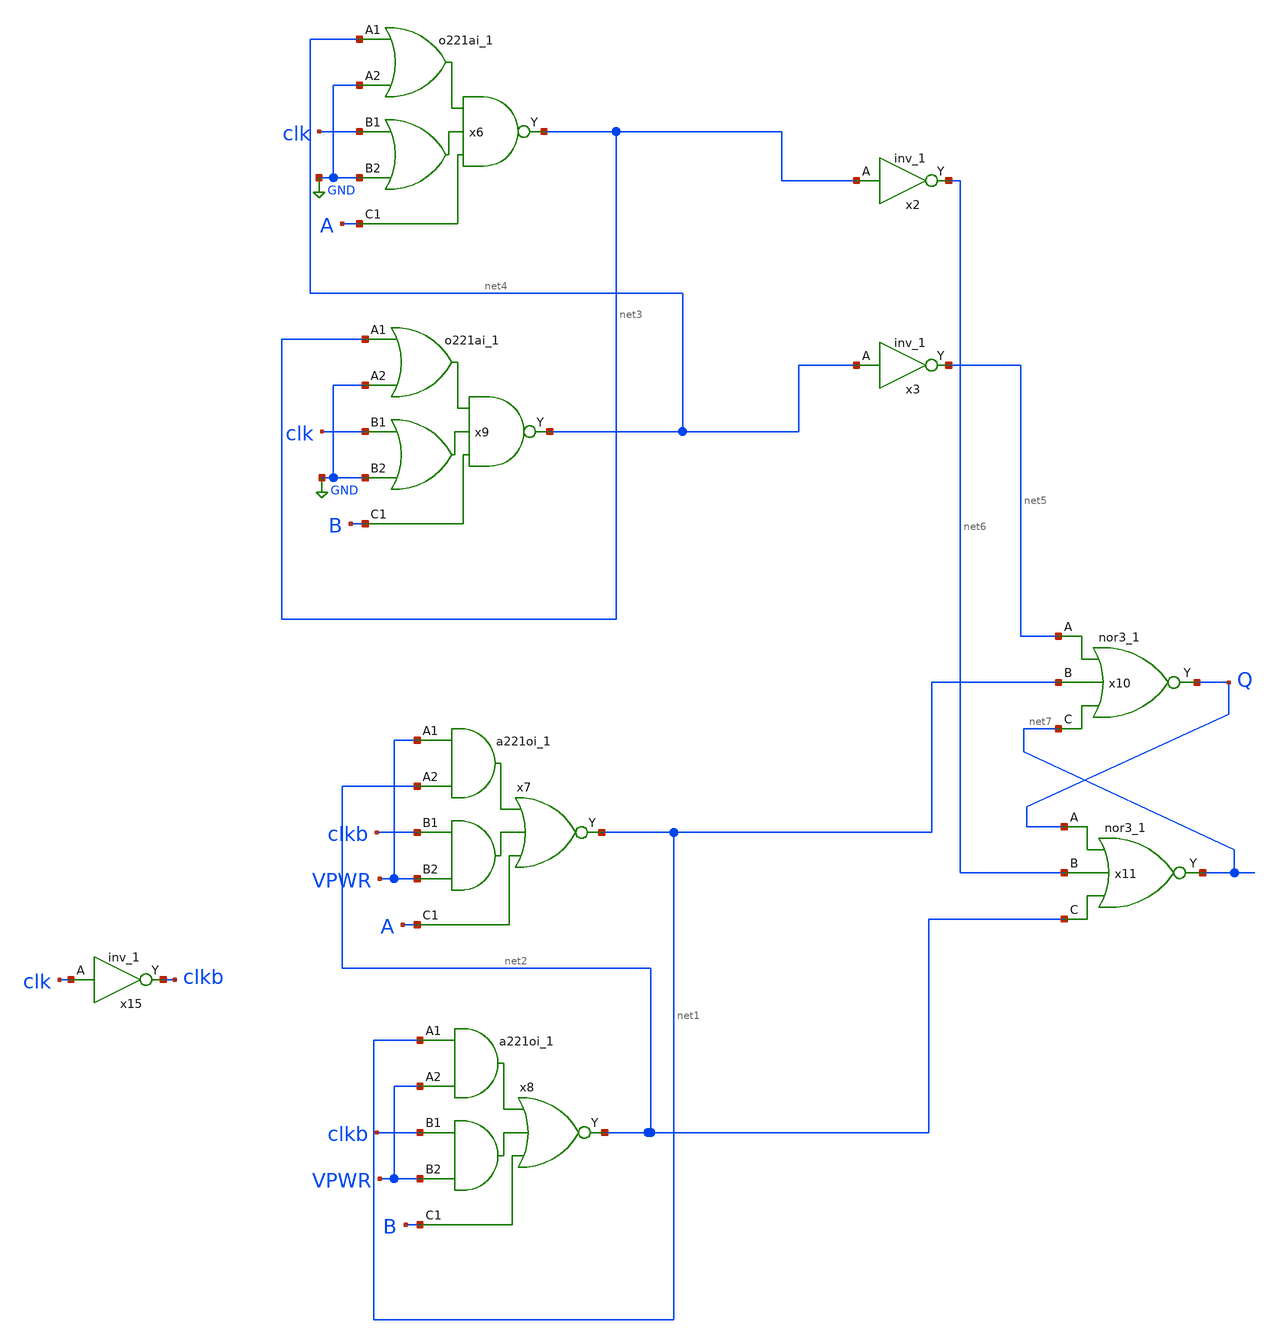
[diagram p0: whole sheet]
** sch_path: Schemtics/ADC/cmp/cmpoai_all__.sch
**.subckt cmpoai_all__
x15 clk VGND VNB VPB VPWR clkb sky130_fd_sc_hd__inv_1
x7 VPWR net2 clkb VPWR A VGND VNB VPB VPWR net1 sky130_fd_sc_hd__a221oi_1
x8 net1 VPWR clkb VPWR B VGND VNB VPB VPWR net2 sky130_fd_sc_hd__a221oi_1
x2 net3 VGND VNB VPB VPWR net6 sky130_fd_sc_hd__inv_1
x3 net4 VGND VNB VPB VPWR net5 sky130_fd_sc_hd__inv_1
x6 net4 GND clk GND A VGND VNB VPB VPWR net3 sky130_fd_sc_hd__o221ai_1
x9 net3 GND clk GND B VGND VNB VPB VPWR net4 sky130_fd_sc_hd__o221ai_1
x10 net5 net1 net7 VGND VNB VPB VPWR Q sky130_fd_sc_hd__nor3_1
x11 Q net6 net2 VGND VNB VPB VPWR net7 sky130_fd_sc_hd__nor3_1
**.ends
.GLOBAL GND
.end
